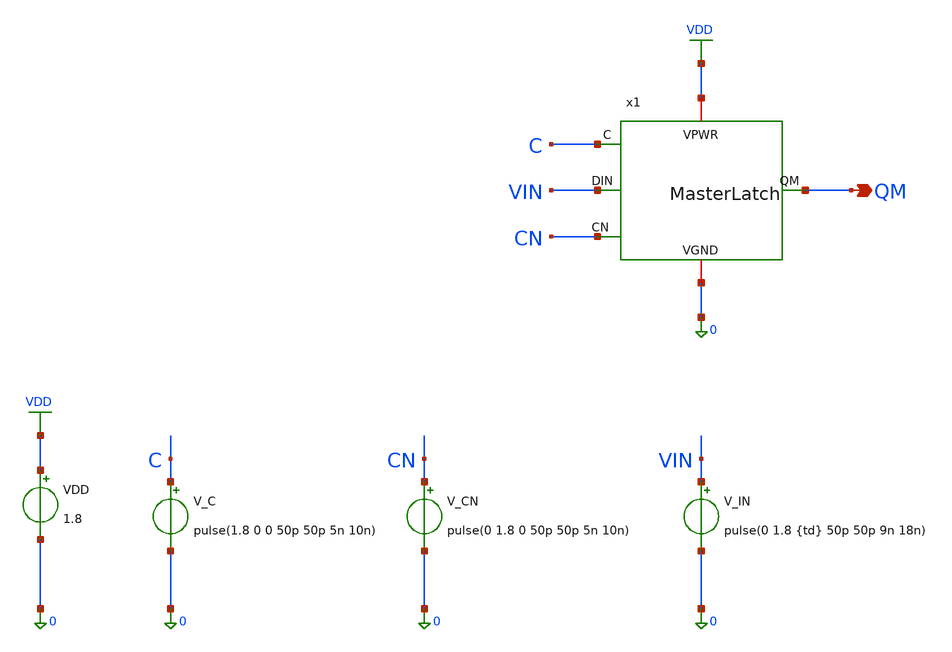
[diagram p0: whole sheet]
** sch_path: latch/MasterLatch_tb_var_delay.sch
**.subckt MasterLatch_tb_var_delay QM
*.opin QM
VDD VDD 0 1.8
V_C C 0 pulse(1.8 0 0 50p 50p 5n 10n)
V_CN CN 0 pulse(0 1.8 0 50p 50p 5n 10n)
V_IN VIN 0 pulse(0 1.8 {td} 50p 50p 9n 18n)
x1 VIN QM C CN VDD 0 MasterLatch
**** begin user architecture code

** opencircuitdesign pdks install
.lib $::SKYWATER_MODELS/sky130.lib.spice tt



.param td=0

.tran 0.001n 11n

.control
  save all
  set filetype=ascii
  shell rm -f /home/sushanth/.xschem/simulations/delay_results.txt

  let td = 5n
  let step = 0.1p

  while td <= 5.05n

    alterparam td = $&td
    reset
    run

    meas tran delay TRIG v(C) VAL=0.9 RISE=1 TARG v(QM) VAL=0.9 RISE=1

    echo $&td,$&delay >> /home/sushanth/.xschem/simulations/delay_results.txt

    let td = td + step

  end

.endc


**** end user architecture code
**.ends
.GLOBAL VDD
.end
